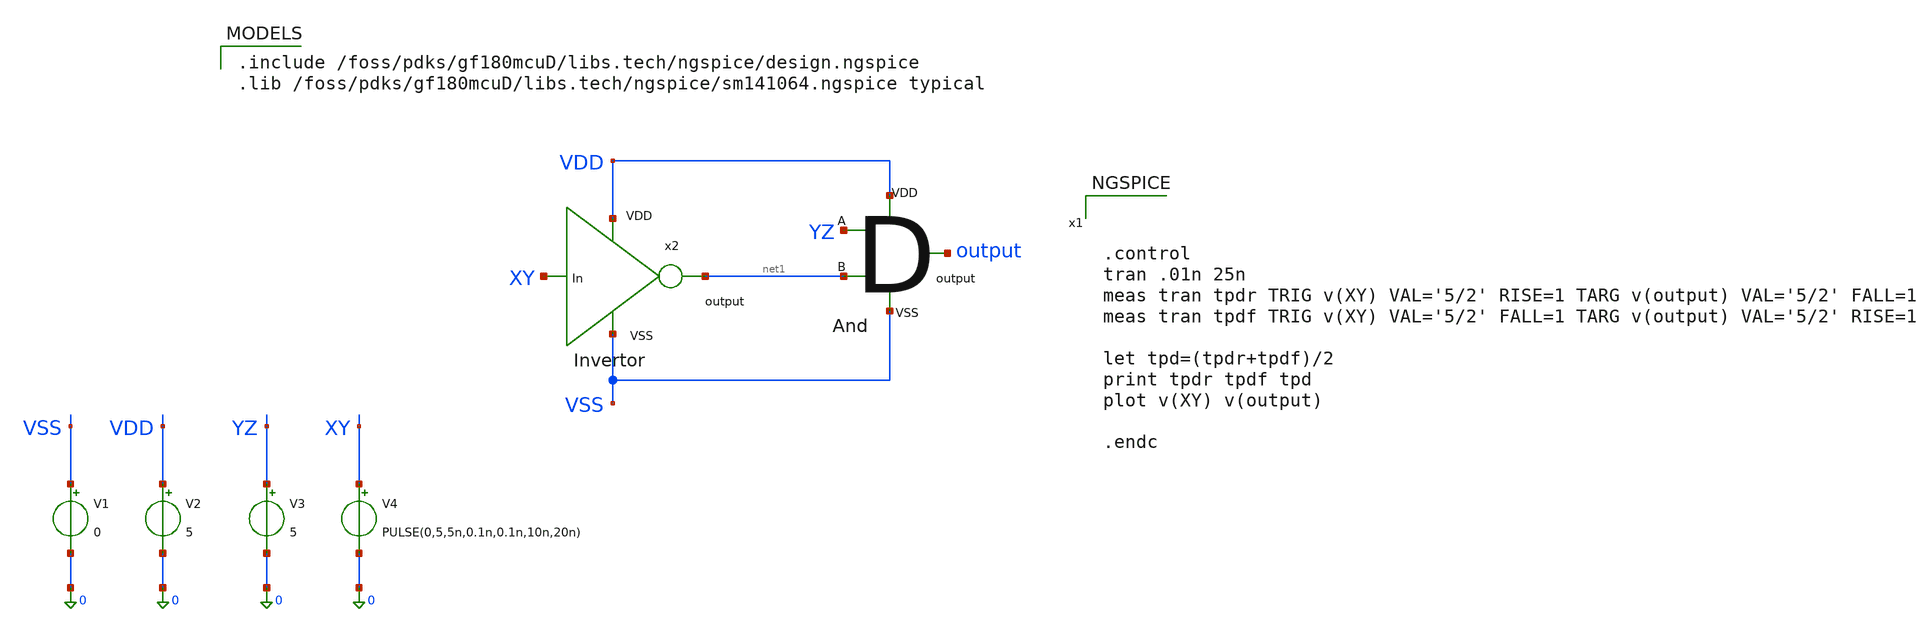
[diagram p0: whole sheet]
** sch_path: activities/opamp3AKAM/yDelayTB.sch
**.subckt yDelayTB
x1 YZ VDD net1 output VSS andGate
x2 VDD net1 XY VSS invertor
V1 VSS 0 0
V2 VDD 0 5
V3 YZ 0 5
V4 XY 0 PULSE(0,5,5n,0.1n,0.1n,10n,20n)
**** begin user architecture code

.include /foss/pdks/gf180mcuD/libs.tech/ngspice/design.ngspice
.lib /foss/pdks/gf180mcuD/libs.tech/ngspice/sm141064.ngspice typical




.control
tran .01n 25n
meas tran tpdr TRIG v(XY) VAL='5/2' RISE=1 TARG v(output) VAL='5/2' FALL=1
meas tran tpdf TRIG v(XY) VAL='5/2' FALL=1 TARG v(output) VAL='5/2' RISE=1

let tpd=(tpdr+tpdf)/2
print tpdr tpdf tpd
plot v(XY) v(output)

.endc


**** end user architecture code
**.ends
.end
